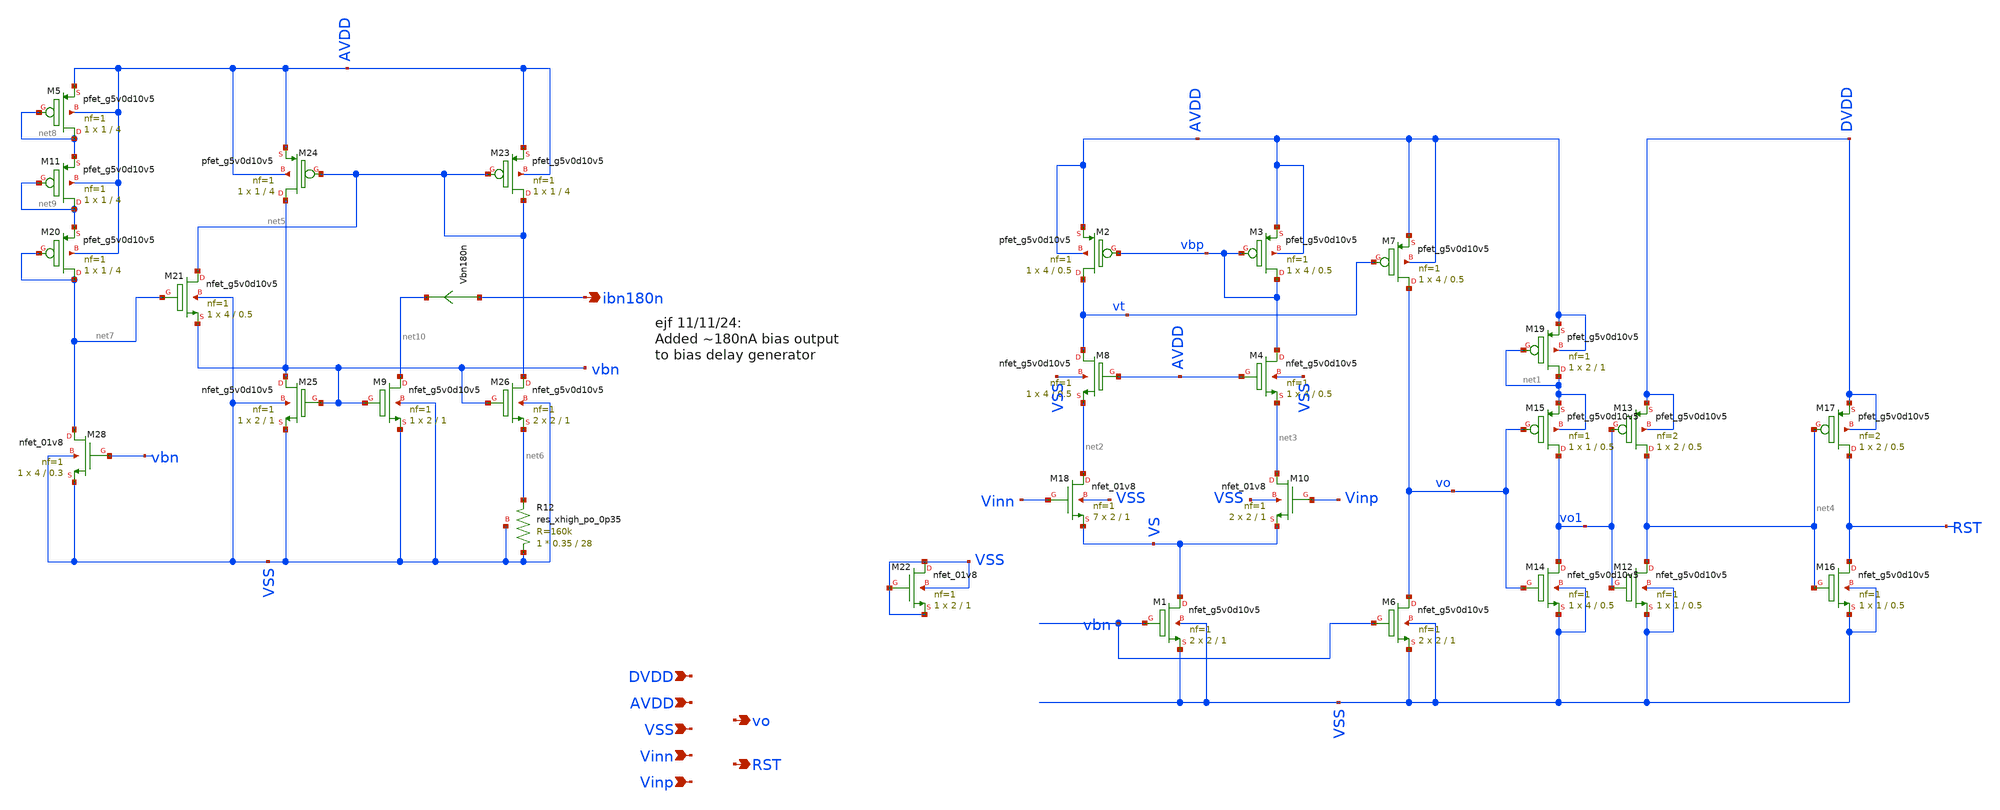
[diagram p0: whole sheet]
** sch_path: xschem/comparator_final.sch
**.subckt comparator_final AVDD RST VSS Vinn Vinp DVDD vo ibn180n
*.ipin AVDD
*.opin RST
*.ipin VSS
*.ipin Vinn
*.ipin Vinp
*.ipin DVDD
*.opin vo
*.opin ibn180n
XM1 VS vbn VSS VSS sky130_fd_pr__nfet_g5v0d10v5 L=1 W=2 nf=1 ad='int((nf+1)/2) * W/nf * 0.29' as='int((nf+2)/2) * W/nf * 0.29'
+ pd='2*int((nf+1)/2) * (W/nf + 0.29)' ps='2*int((nf+2)/2) * (W/nf + 0.29)' nrd='0.29 / W' nrs='0.29 / W'
+ sa=0 sb=0 sd=0 mult=2 m=2
XM3 vbp vbp AVDD AVDD sky130_fd_pr__pfet_g5v0d10v5 L=0.5 W=4 nf=1 ad='int((nf+1)/2) * W/nf * 0.29' as='int((nf+2)/2) * W/nf * 0.29'
+ pd='2*int((nf+1)/2) * (W/nf + 0.29)' ps='2*int((nf+2)/2) * (W/nf + 0.29)' nrd='0.29 / W' nrs='0.29 / W'
+ sa=0 sb=0 sd=0 mult=1 m=1
XM2 vt vbp AVDD AVDD sky130_fd_pr__pfet_g5v0d10v5 L=0.5 W=4 nf=1 ad='int((nf+1)/2) * W/nf * 0.29' as='int((nf+2)/2) * W/nf * 0.29'
+ pd='2*int((nf+1)/2) * (W/nf + 0.29)' ps='2*int((nf+2)/2) * (W/nf + 0.29)' nrd='0.29 / W' nrs='0.29 / W'
+ sa=0 sb=0 sd=0 mult=1 m=1
XM7 vo vt AVDD AVDD sky130_fd_pr__pfet_g5v0d10v5 L=0.5 W=4 nf=1 ad='int((nf+1)/2) * W/nf * 0.29' as='int((nf+2)/2) * W/nf * 0.29'
+ pd='2*int((nf+1)/2) * (W/nf + 0.29)' ps='2*int((nf+2)/2) * (W/nf + 0.29)' nrd='0.29 / W' nrs='0.29 / W'
+ sa=0 sb=0 sd=0 mult=1 m=1
XM6 vo vbn VSS VSS sky130_fd_pr__nfet_g5v0d10v5 L=1 W=2 nf=1 ad='int((nf+1)/2) * W/nf * 0.29' as='int((nf+2)/2) * W/nf * 0.29'
+ pd='2*int((nf+1)/2) * (W/nf + 0.29)' ps='2*int((nf+2)/2) * (W/nf + 0.29)' nrd='0.29 / W' nrs='0.29 / W'
+ sa=0 sb=0 sd=0 mult=2 m=2
XM14 vo1 vo VSS VSS sky130_fd_pr__nfet_g5v0d10v5 L=0.5 W=4 nf=1 ad='int((nf+1)/2) * W/nf * 0.29' as='int((nf+2)/2) * W/nf * 0.29'
+ pd='2*int((nf+1)/2) * (W/nf + 0.29)' ps='2*int((nf+2)/2) * (W/nf + 0.29)' nrd='0.29 / W' nrs='0.29 / W'
+ sa=0 sb=0 sd=0 mult=1 m=1
XM15 vo1 vo net1 net1 sky130_fd_pr__pfet_g5v0d10v5 L=0.5 W=1 nf=1 ad='int((nf+1)/2) * W/nf * 0.29' as='int((nf+2)/2) * W/nf * 0.29'
+ pd='2*int((nf+1)/2) * (W/nf + 0.29)' ps='2*int((nf+2)/2) * (W/nf + 0.29)' nrd='0.29 / W' nrs='0.29 / W'
+ sa=0 sb=0 sd=0 mult=1 m=1
XM12 net4 vo1 VSS VSS sky130_fd_pr__nfet_g5v0d10v5 L=0.5 W=1 nf=1 ad='int((nf+1)/2) * W/nf * 0.29' as='int((nf+2)/2) * W/nf * 0.29'
+ pd='2*int((nf+1)/2) * (W/nf + 0.29)' ps='2*int((nf+2)/2) * (W/nf + 0.29)' nrd='0.29 / W' nrs='0.29 / W'
+ sa=0 sb=0 sd=0 mult=1 m=1
XM13 net4 vo1 DVDD DVDD sky130_fd_pr__pfet_g5v0d10v5 L=0.5 W=2 nf=2 ad='int((nf+1)/2) * W/nf * 0.29'
+ as='int((nf+2)/2) * W/nf * 0.29' pd='2*int((nf+1)/2) * (W/nf + 0.29)' ps='2*int((nf+2)/2) * (W/nf + 0.29)'
+ nrd='0.29 / W' nrs='0.29 / W' sa=0 sb=0 sd=0 mult=1 m=1
XM16 RST net4 VSS VSS sky130_fd_pr__nfet_g5v0d10v5 L=0.5 W=1 nf=1 ad='int((nf+1)/2) * W/nf * 0.29' as='int((nf+2)/2) * W/nf * 0.29'
+ pd='2*int((nf+1)/2) * (W/nf + 0.29)' ps='2*int((nf+2)/2) * (W/nf + 0.29)' nrd='0.29 / W' nrs='0.29 / W'
+ sa=0 sb=0 sd=0 mult=1 m=1
XM17 RST net4 DVDD DVDD sky130_fd_pr__pfet_g5v0d10v5 L=0.5 W=2 nf=2 ad='int((nf+1)/2) * W/nf * 0.29'
+ as='int((nf+2)/2) * W/nf * 0.29' pd='2*int((nf+1)/2) * (W/nf + 0.29)' ps='2*int((nf+2)/2) * (W/nf + 0.29)'
+ nrd='0.29 / W' nrs='0.29 / W' sa=0 sb=0 sd=0 mult=1 m=1
XM4 vbp AVDD net3 VSS sky130_fd_pr__nfet_g5v0d10v5 L=0.5 W=4 nf=1 ad='int((nf+1)/2) * W/nf * 0.29' as='int((nf+2)/2) * W/nf * 0.29'
+ pd='2*int((nf+1)/2) * (W/nf + 0.29)' ps='2*int((nf+2)/2) * (W/nf + 0.29)' nrd='0.29 / W' nrs='0.29 / W'
+ sa=0 sb=0 sd=0 mult=1 m=1
XM8 vt AVDD net2 VSS sky130_fd_pr__nfet_g5v0d10v5 L=0.5 W=4 nf=1 ad='int((nf+1)/2) * W/nf * 0.29' as='int((nf+2)/2) * W/nf * 0.29'
+ pd='2*int((nf+1)/2) * (W/nf + 0.29)' ps='2*int((nf+2)/2) * (W/nf + 0.29)' nrd='0.29 / W' nrs='0.29 / W'
+ sa=0 sb=0 sd=0 mult=1 m=1
XM19 net1 net1 AVDD AVDD sky130_fd_pr__pfet_g5v0d10v5 L=1 W=2 nf=1 ad='int((nf+1)/2) * W/nf * 0.29' as='int((nf+2)/2) * W/nf * 0.29'
+ pd='2*int((nf+1)/2) * (W/nf + 0.29)' ps='2*int((nf+2)/2) * (W/nf + 0.29)' nrd='0.29 / W' nrs='0.29 / W'
+ sa=0 sb=0 sd=0 mult=1 m=1
XM23 net5 net5 AVDD AVDD sky130_fd_pr__pfet_g5v0d10v5 L=4 W=1 nf=1 ad='int((nf+1)/2) * W/nf * 0.29' as='int((nf+2)/2) * W/nf * 0.29'
+ pd='2*int((nf+1)/2) * (W/nf + 0.29)' ps='2*int((nf+2)/2) * (W/nf + 0.29)' nrd='0.29 / W' nrs='0.29 / W'
+ sa=0 sb=0 sd=0 mult=1 m=1
XM24 vbn net5 AVDD AVDD sky130_fd_pr__pfet_g5v0d10v5 L=4 W=1 nf=1 ad='int((nf+1)/2) * W/nf * 0.29' as='int((nf+2)/2) * W/nf * 0.29'
+ pd='2*int((nf+1)/2) * (W/nf + 0.29)' ps='2*int((nf+2)/2) * (W/nf + 0.29)' nrd='0.29 / W' nrs='0.29 / W'
+ sa=0 sb=0 sd=0 mult=1 m=1
XR12 VSS net6 VSS sky130_fd_pr__res_xhigh_po_0p35 L=28 mult=1 m=1
XM25 vbn vbn VSS VSS sky130_fd_pr__nfet_g5v0d10v5 L=1 W=2 nf=1 ad='int((nf+1)/2) * W/nf * 0.29' as='int((nf+2)/2) * W/nf * 0.29'
+ pd='2*int((nf+1)/2) * (W/nf + 0.29)' ps='2*int((nf+2)/2) * (W/nf + 0.29)' nrd='0.29 / W' nrs='0.29 / W'
+ sa=0 sb=0 sd=0 mult=1 m=1
XM26 net5 vbn net6 VSS sky130_fd_pr__nfet_g5v0d10v5 L=1 W=2 nf=1 ad='int((nf+1)/2) * W/nf * 0.29' as='int((nf+2)/2) * W/nf * 0.29'
+ pd='2*int((nf+1)/2) * (W/nf + 0.29)' ps='2*int((nf+2)/2) * (W/nf + 0.29)' nrd='0.29 / W' nrs='0.29 / W'
+ sa=0 sb=0 sd=0 mult=2 m=2
XM28 net7 vbn VSS VSS sky130_fd_pr__nfet_01v8 L=0.3 W=4 nf=1 ad='int((nf+1)/2) * W/nf * 0.29' as='int((nf+2)/2) * W/nf * 0.29'
+ pd='2*int((nf+1)/2) * (W/nf + 0.29)' ps='2*int((nf+2)/2) * (W/nf + 0.29)' nrd='0.29 / W' nrs='0.29 / W'
+ sa=0 sb=0 sd=0 mult=1 m=1
XM18 net2 Vinn VS VSS sky130_fd_pr__nfet_01v8 L=1 W=2 nf=1 ad='int((nf+1)/2) * W/nf * 0.29' as='int((nf+2)/2) * W/nf * 0.29'
+ pd='2*int((nf+1)/2) * (W/nf + 0.29)' ps='2*int((nf+2)/2) * (W/nf + 0.29)' nrd='0.29 / W' nrs='0.29 / W'
+ sa=0 sb=0 sd=0 mult=7 m=7
XM10 net3 Vinp VS VSS sky130_fd_pr__nfet_01v8 L=1 W=2 nf=1 ad='int((nf+1)/2) * W/nf * 0.29' as='int((nf+2)/2) * W/nf * 0.29'
+ pd='2*int((nf+1)/2) * (W/nf + 0.29)' ps='2*int((nf+2)/2) * (W/nf + 0.29)' nrd='0.29 / W' nrs='0.29 / W'
+ sa=0 sb=0 sd=0 mult=2 m=2
XM5 net8 net8 AVDD AVDD sky130_fd_pr__pfet_g5v0d10v5 L=4 W=1 nf=1 ad='int((nf+1)/2) * W/nf * 0.29' as='int((nf+2)/2) * W/nf * 0.29'
+ pd='2*int((nf+1)/2) * (W/nf + 0.29)' ps='2*int((nf+2)/2) * (W/nf + 0.29)' nrd='0.29 / W' nrs='0.29 / W'
+ sa=0 sb=0 sd=0 mult=1 m=1
XM11 net9 net9 net8 AVDD sky130_fd_pr__pfet_g5v0d10v5 L=4 W=1 nf=1 ad='int((nf+1)/2) * W/nf * 0.29' as='int((nf+2)/2) * W/nf * 0.29'
+ pd='2*int((nf+1)/2) * (W/nf + 0.29)' ps='2*int((nf+2)/2) * (W/nf + 0.29)' nrd='0.29 / W' nrs='0.29 / W'
+ sa=0 sb=0 sd=0 mult=1 m=1
XM20 net7 net7 net9 AVDD sky130_fd_pr__pfet_g5v0d10v5 L=4 W=1 nf=1 ad='int((nf+1)/2) * W/nf * 0.29' as='int((nf+2)/2) * W/nf * 0.29'
+ pd='2*int((nf+1)/2) * (W/nf + 0.29)' ps='2*int((nf+2)/2) * (W/nf + 0.29)' nrd='0.29 / W' nrs='0.29 / W'
+ sa=0 sb=0 sd=0 mult=1 m=1
XM21 net5 net7 vbn VSS sky130_fd_pr__nfet_g5v0d10v5 L=0.5 W=4 nf=1 ad='int((nf+1)/2) * W/nf * 0.29' as='int((nf+2)/2) * W/nf * 0.29'
+ pd='2*int((nf+1)/2) * (W/nf + 0.29)' ps='2*int((nf+2)/2) * (W/nf + 0.29)' nrd='0.29 / W' nrs='0.29 / W'
+ sa=0 sb=0 sd=0 mult=1 m=1
XM9 net10 vbn VSS VSS sky130_fd_pr__nfet_g5v0d10v5 L=1 W=2 nf=1 ad='int((nf+1)/2) * W/nf * 0.29' as='int((nf+2)/2) * W/nf * 0.29'
+ pd='2*int((nf+1)/2) * (W/nf + 0.29)' ps='2*int((nf+2)/2) * (W/nf + 0.29)' nrd='0.29 / W' nrs='0.29 / W'
+ sa=0 sb=0 sd=0 mult=1 m=1
Vbn180n ibn180n net10 0
.save i(vbn180n)
XM22 VSS VSS VSS VSS sky130_fd_pr__nfet_01v8 L=1 W=2 nf=1 ad='int((nf+1)/2) * W/nf * 0.29' as='int((nf+2)/2) * W/nf * 0.29'
+ pd='2*int((nf+1)/2) * (W/nf + 0.29)' ps='2*int((nf+2)/2) * (W/nf + 0.29)' nrd='0.29 / W' nrs='0.29 / W'
+ sa=0 sb=0 sd=0 mult=1 m=1
**.ends
.end
